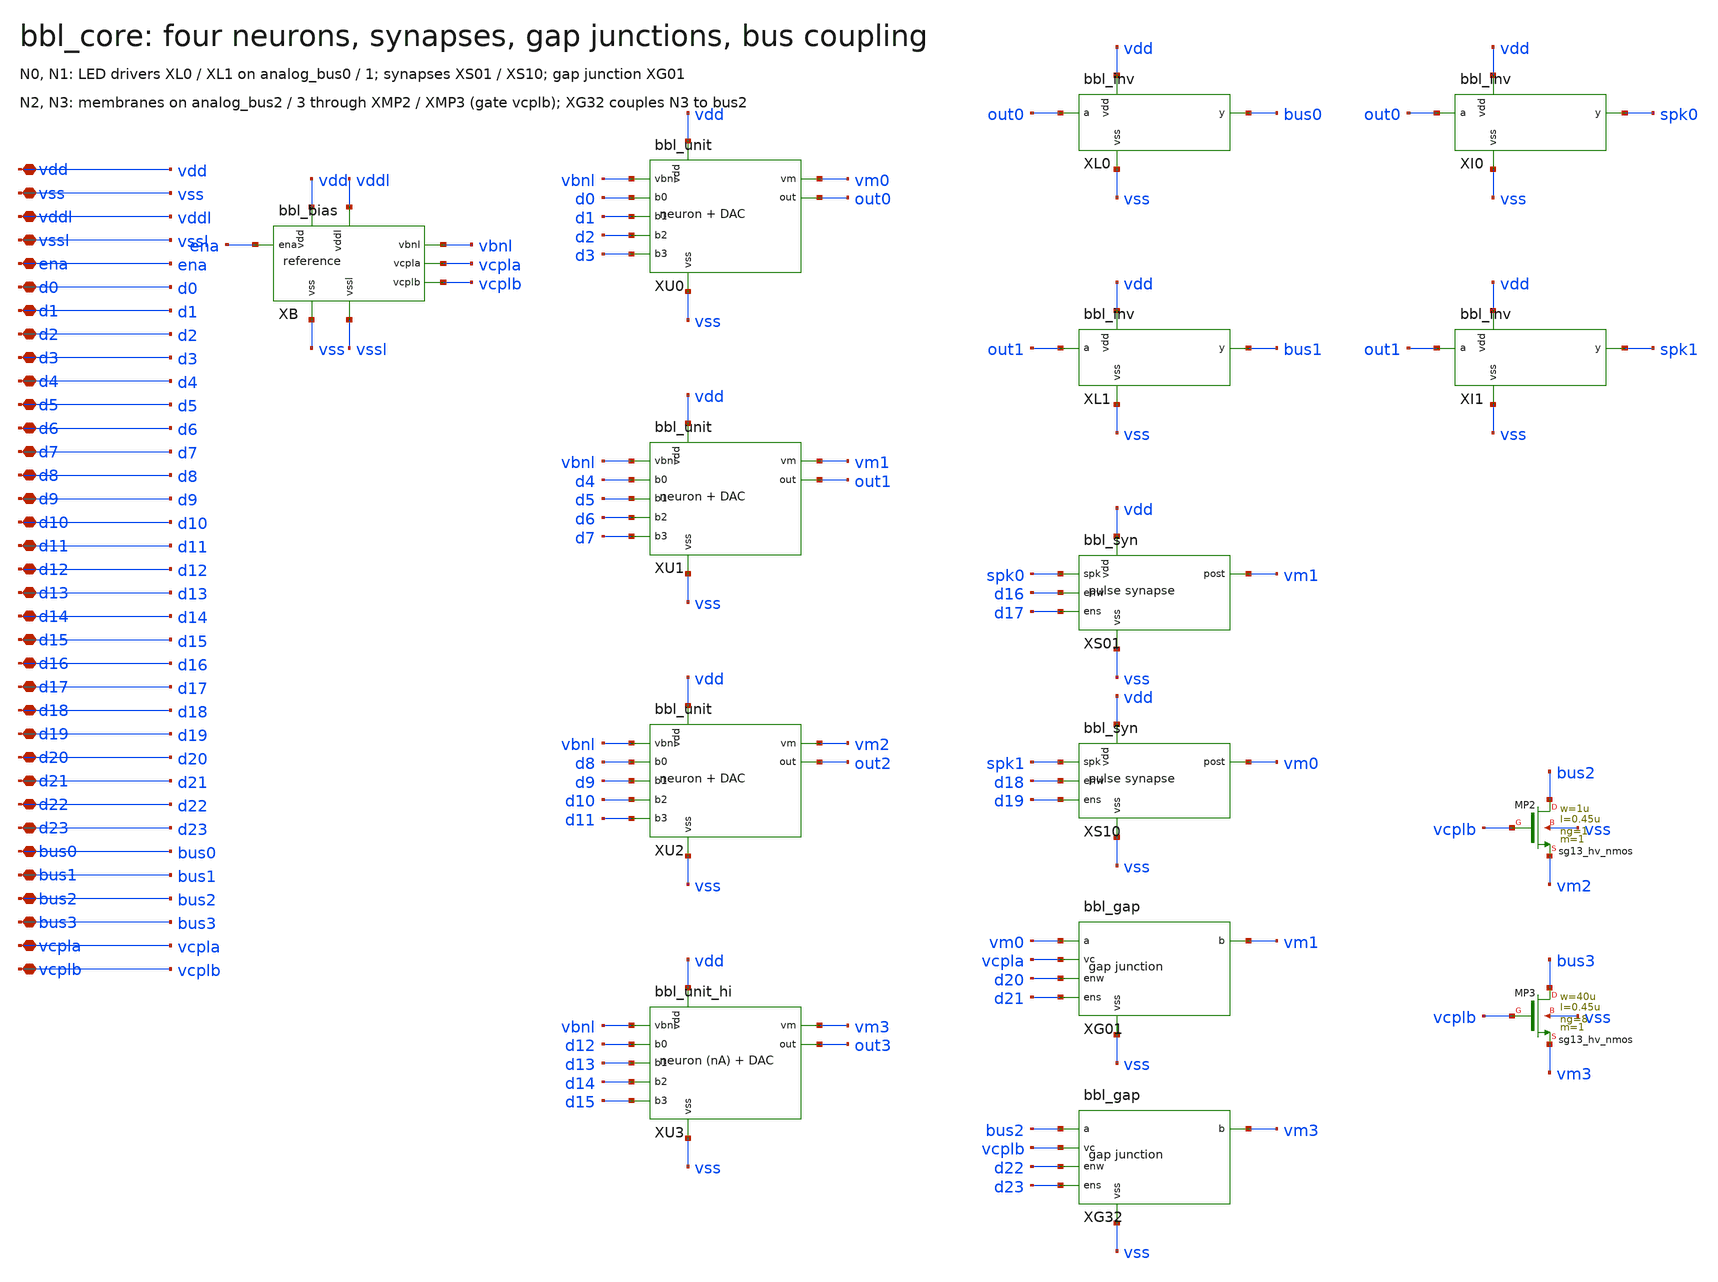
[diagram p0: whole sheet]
** sch_path: schematic/xschem/bbl_core.sch
**.subckt bbl_core vdd vss vddl vssl ena d0 d1 d2 d3 d4 d5 d6 d7 d8 d9 d10 d11 d12 d13 d14 d15 d16
*+ d17 d18 d19 d20 d21 d22 d23 bus0 bus1 bus2 bus3 vcpla vcplb
*.iopin vdd
*.iopin vss
*.iopin vddl
*.iopin vssl
*.iopin ena
*.iopin d0
*.iopin d1
*.iopin d2
*.iopin d3
*.iopin d4
*.iopin d5
*.iopin d6
*.iopin d7
*.iopin d8
*.iopin d9
*.iopin d10
*.iopin d11
*.iopin d12
*.iopin d13
*.iopin d14
*.iopin d15
*.iopin d16
*.iopin d17
*.iopin d18
*.iopin d19
*.iopin d20
*.iopin d21
*.iopin d22
*.iopin d23
*.iopin bus0
*.iopin bus1
*.iopin bus2
*.iopin bus3
*.iopin vcpla
*.iopin vcplb
XB vdd vss vddl vssl ena vbnl vcpla vcplb bbl_bias
XU0 vdd vss vm0 out0 vbnl d0 d1 d2 d3 bbl_unit
XU1 vdd vss vm1 out1 vbnl d4 d5 d6 d7 bbl_unit
XU2 vdd vss vm2 out2 vbnl d8 d9 d10 d11 bbl_unit
XU3 vdd vss vm3 out3 vbnl d12 d13 d14 d15 bbl_unit_hi
XL0 vdd vss out0 bus0 bbl_inv
XL1 vdd vss out1 bus1 bbl_inv
XI0 vdd vss out0 spk0 bbl_inv
XI1 vdd vss out1 spk1 bbl_inv
XS01 vdd vss spk0 vm1 d16 d17 bbl_syn
XS10 vdd vss spk1 vm0 d18 d19 bbl_syn
XG01 vss vm0 vm1 vcpla d20 d21 bbl_gap
XG32 vss bus2 vm3 vcplb d22 d23 bbl_gap
XMP2 bus2 vcplb vm2 vss sg13_hv_nmos w=1u l=0.45u ng=1 m=1 mm_ok=1
XMP3 bus3 vcplb vm3 vss sg13_hv_nmos w=40u l=0.45u ng=8 m=1 mm_ok=1
**.ends

* expanding   symbol:  bbl_bias.sym # of pins=8
** sym_path: schematic/xschem/bbl_bias.sym
** sch_path: schematic/xschem/bbl_bias.sch
.subckt bbl_bias vdd vss vddl vssl ena vbnl vcpla vcplb
*.iopin vdd
*.iopin vss
*.iopin vddl
*.iopin vssl
*.iopin ena
*.iopin vbnl
*.iopin vcpla
*.iopin vcplb
XMIP enab ena vddl vddl sg13_lv_pmos w=0.3u l=0.5u ng=1 m=1 mm_ok=1
XMPA vbn vbp vdd vdd sg13_hv_pmos w=2u l=2u ng=1 m=1 mm_ok=1
XMPB vbp vbp vdd vdd sg13_hv_pmos w=2u l=2u ng=1 m=1 mm_ok=1
XMSU vbn vdd vdd vdd sg13_hv_pmos w=4u l=0.45u ng=1 m=1 mm_ok=1
XMLP vbnl vbp vdd vdd sg13_hv_pmos w=0.3u l=8u ng=1 m=1 mm_ok=1
XMCA vcpla vbp vdd vdd sg13_hv_pmos w=0.3u l=22u ng=1 m=1 mm_ok=1
XMCB vcplb vbp vdd vdd sg13_hv_pmos w=0.3u l=22u ng=1 m=1 mm_ok=1
XMIN enab ena vssl vss sg13_lv_nmos w=0.3u l=0.5u ng=1 m=1 mm_ok=1
XMNA vbn vbn sa vss sg13_hv_nmos w=2u l=2u ng=1 m=1 mm_ok=1
XMNB vbp vbn rs vss sg13_hv_nmos w=16u l=2u ng=8 m=1 mm_ok=1
XMCL vbn enab vss vss sg13_hv_nmos w=1u l=0.45u ng=1 m=1 mm_ok=1
XMLD vbnl vbnl vss vss sg13_hv_nmos w=2u l=2u ng=1 m=1 mm_ok=1
XCA vss vcpla vss vss sg13_hv_nmos w=50u l=10u ng=5 m=1 mm_ok=1
XCB vss vcplb vss vss sg13_hv_nmos w=50u l=10u ng=5 m=1 mm_ok=1
XMEA sa ena vss vss sg13_hv_nmos w=1u l=0.45u ng=1 m=1 mm_ok=1
XR1 rs sb vss rhigh w=0.5e-6 l=41.055e-6 m=1 b=9 mm_ok=1
XMEB sb ena vss vss sg13_hv_nmos w=1u l=0.45u ng=1 m=1 mm_ok=1
.ends


* expanding   symbol:  bbl_unit.sym # of pins=9
** sym_path: schematic/xschem/bbl_unit.sym
** sch_path: schematic/xschem/bbl_unit.sch
.subckt bbl_unit vdd vss vm out vbnl b0 b1 b2 b3
*.iopin vdd
*.iopin vss
*.iopin vm
*.iopin out
*.iopin vbnl
*.iopin b0
*.iopin b1
*.iopin b2
*.iopin b3
XN vdd vss vm out vin bbl_neuron
XD vdd vss vin vbnl b0 b1 b2 b3 bbl_dac
.ends


* expanding   symbol:  bbl_unit_hi.sym # of pins=9
** sym_path: schematic/xschem/bbl_unit_hi.sym
** sch_path: schematic/xschem/bbl_unit_hi.sch
.subckt bbl_unit_hi vdd vss vm out vbnl b0 b1 b2 b3
*.iopin vdd
*.iopin vss
*.iopin vm
*.iopin out
*.iopin vbnl
*.iopin b0
*.iopin b1
*.iopin b2
*.iopin b3
XN vdd vss vm out vin bbl_neuron_hi
XD vdd vss vin vbnl b0 b1 b2 b3 bbl_dac
.ends


* expanding   symbol:  bbl_inv.sym # of pins=4
** sym_path: schematic/xschem/bbl_inv.sym
** sch_path: schematic/xschem/bbl_inv.sch
.subckt bbl_inv vdd vss a y
*.iopin vdd
*.iopin vss
*.iopin a
*.iopin y
XMP y a vdd vdd sg13_hv_pmos w=1u l=0.45u ng=1 m=1 mm_ok=1
XMN y a vss vss sg13_hv_nmos w=1u l=0.45u ng=1 m=1 mm_ok=1
.ends


* expanding   symbol:  bbl_syn.sym # of pins=6
** sym_path: schematic/xschem/bbl_syn.sym
** sch_path: schematic/xschem/bbl_syn.sch
.subckt bbl_syn vdd vss spk post enw ens
*.iopin vdd
*.iopin vss
*.iopin spk
*.iopin post
*.iopin enw
*.iopin ens
XMPW gw spk vdd vdd sg13_hv_pmos w=0.3u l=0.45u ng=1 m=1 mm_ok=1
XMRW gw vss vdd vdd sg13_hv_pmos w=0.3u l=20u ng=1 m=1 mm_ok=1
XMSW post gw vdd vdd sg13_hv_pmos w=0.3u l=100u ng=1 m=1 mm_ok=1
XMPS gs spk vdd vdd sg13_hv_pmos w=0.3u l=0.45u ng=1 m=1 mm_ok=1
XMRS gs vss vdd vdd sg13_hv_pmos w=0.3u l=20u ng=1 m=1 mm_ok=1
XMSS post gs vdd vdd sg13_hv_pmos w=0.3u l=20u ng=1 m=1 mm_ok=1
XMNW gw enw bw vss sg13_hv_nmos w=0.3u l=0.45u ng=1 m=1 mm_ok=1
XMNS gs ens bs vss sg13_hv_nmos w=0.3u l=0.45u ng=1 m=1 mm_ok=1
XMBW bw spk vss vss sg13_hv_nmos w=0.3u l=0.45u ng=1 m=1 mm_ok=1
XMBS bs spk vss vss sg13_hv_nmos w=0.3u l=0.45u ng=1 m=1 mm_ok=1
.ends


* expanding   symbol:  bbl_gap.sym # of pins=6
** sym_path: schematic/xschem/bbl_gap.sym
** sch_path: schematic/xschem/bbl_gap.sch
.subckt bbl_gap vss a b vc enw ens
*.iopin vss
*.iopin a
*.iopin b
*.iopin vc
*.iopin enw
*.iopin ens
XMGW a vc gw vss sg13_hv_nmos w=0.3u l=10u ng=1 m=1 mm_ok=1
XMGS a vc gs vss sg13_hv_nmos w=1u l=0.45u ng=1 m=1 mm_ok=1
XMTW gw enw b vss sg13_hv_nmos w=0.3u l=0.45u ng=1 m=1 mm_ok=1
XMTS gs ens b vss sg13_hv_nmos w=1u l=0.45u ng=1 m=1 mm_ok=1
.ends


* expanding   symbol:  bbl_neuron.sym # of pins=5
** sym_path: schematic/xschem/bbl_neuron.sym
** sch_path: schematic/xschem/bbl_neuron.sch
.subckt bbl_neuron vdd vss vm out vin
*.iopin vdd
*.iopin vss
*.iopin vm
*.iopin out
*.iopin vin
XMR3 vm vin vdd vdd sg13_hv_pmos w=0.3u l=30u ng=1 m=1 mm_ok=1
XC1 vdd vm vdd vdd sg13_hv_pmos w=225u l=10u ng=18 m=1 mm_ok=1
XM3 vm out vdd vdd sg13_hv_pmos w=1u l=0.45u ng=1 m=1 mm_ok=1
XMR1 out vss vdd vdd sg13_hv_pmos w=0.3u l=20u ng=1 m=1 mm_ok=1
XM4 rst slow vdd vdd sg13_hv_pmos w=1u l=0.45u ng=1 m=1 mm_ok=1
XMR5 slow vss out vdd sg13_hv_pmos w=0.3u l=100u ng=1 m=1 mm_ok=1
XM2 vm rst vss vss sg13_hv_nmos w=2u l=0.45u ng=1 m=1 mm_ok=1
XM1 out vm vss vss sg13_hv_nmos w=1u l=1u ng=1 m=1 mm_ok=1
XMR2 rst vdd vss vss sg13_hv_nmos w=0.3u l=20u ng=1 m=1 mm_ok=1
XC2 vss slow vss vss sg13_hv_nmos w=40u l=10u ng=4 m=1 mm_ok=1
.ends


* expanding   symbol:  bbl_dac.sym # of pins=8
** sym_path: schematic/xschem/bbl_dac.sym
** sch_path: schematic/xschem/bbl_dac.sch
.subckt bbl_dac vdd vss vin vbnl b0 b1 b2 b3
*.iopin vdd
*.iopin vss
*.iopin vin
*.iopin vbnl
*.iopin b0
*.iopin b1
*.iopin b2
*.iopin b3
XMD vin vin vdd vdd sg13_hv_pmos w=3u l=3u ng=1 m=1 mm_ok=1
XMH vin vbnl vss vss sg13_hv_nmos w=0.3u l=9u ng=1 m=1 mm_ok=1
XMU0 vin vbnl s0 vss sg13_hv_nmos w=0.3u l=2u ng=1 m=1 mm_ok=1
XMU1 vin vbnl s1 vss sg13_hv_nmos w=0.6u l=2u ng=2 m=1 mm_ok=1
XMU2 vin vbnl s2 vss sg13_hv_nmos w=1.2u l=2u ng=4 m=1 mm_ok=1
XMU3 vin vbnl s3 vss sg13_hv_nmos w=2.4u l=2u ng=8 m=1 mm_ok=1
XMS0 s0 b0 vss vss sg13_hv_nmos w=0.3u l=0.45u ng=1 m=1 mm_ok=1
XMS1 s1 b1 vss vss sg13_hv_nmos w=0.6u l=0.45u ng=2 m=1 mm_ok=1
XMS2 s2 b2 vss vss sg13_hv_nmos w=1.2u l=0.45u ng=4 m=1 mm_ok=1
XMS3 s3 b3 vss vss sg13_hv_nmos w=2.4u l=0.45u ng=8 m=1 mm_ok=1
.ends


* expanding   symbol:  bbl_neuron_hi.sym # of pins=5
** sym_path: schematic/xschem/bbl_neuron_hi.sym
** sch_path: schematic/xschem/bbl_neuron_hi.sch
.subckt bbl_neuron_hi vdd vss vm out vin
*.iopin vdd
*.iopin vss
*.iopin vm
*.iopin out
*.iopin vin
XMR3 vm vin vdd vdd sg13_hv_pmos w=48u l=3u ng=8 m=1 mm_ok=1
XC1 vdd vm vdd vdd sg13_hv_pmos w=225u l=10u ng=18 m=1 mm_ok=1
XM2 vm rst vss vss sg13_hv_nmos w=40u l=0.45u ng=8 m=1 mm_ok=1
XM3 vm out vdd vdd sg13_hv_pmos w=0.3u l=4u ng=1 m=1 mm_ok=1
XMR1 out vss vdd vdd sg13_hv_pmos w=0.3u l=20u ng=1 m=1 mm_ok=1
XM1 out vm vss vss sg13_hv_nmos w=1u l=1u ng=1 m=1 mm_ok=1
XMR5A slow outb vss vss sg13_hv_nmos w=3u l=0.45u ng=1 m=1 mm_ok=1
XMR5B slow vin vdd vdd sg13_hv_pmos w=10u l=0.45u ng=2 m=1 mm_ok=1
XC2 vss slow vss vss sg13_hv_nmos w=60u l=10u ng=6 m=1 mm_ok=1
XM4 rst slow vdd vdd sg13_hv_pmos w=10u l=0.45u ng=2 m=1 mm_ok=1
XMR2 rst vdd vss vss sg13_hv_nmos w=0.3u l=20u ng=1 m=1 mm_ok=1
XMQ out outb vdd vdd sg13_hv_pmos w=0.3u l=3u ng=1 m=1 mm_ok=1
XMIP outb out vdd vdd sg13_hv_pmos w=3u l=0.45u ng=1 m=1 mm_ok=1
XMIN outb out vss vss sg13_hv_nmos w=0.3u l=4u ng=1 m=1 mm_ok=1
.ends

.end
